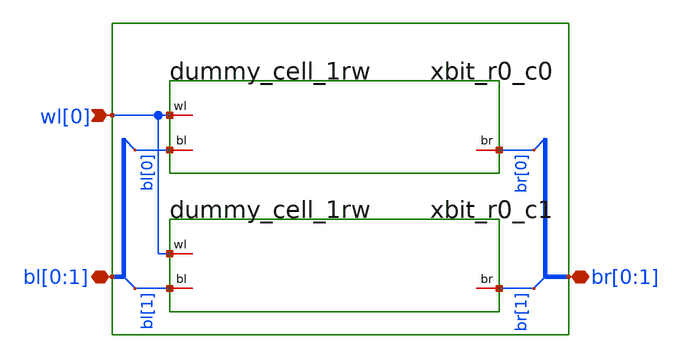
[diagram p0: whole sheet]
** sch_path: sram_2_16_scn4m/dummy_array_1.sch
**.subckt dummy_array_1 bl[0],bl[1] br[0],br[1] wl[0]
*.iopin bl[0],bl[1]
*.iopin br[0],br[1]
*.ipin wl[0]
xbit_r0_c0 bl[0] br[0] wl[0] vdd gnd dummy_cell_1rw
xbit_r0_c1 bl[1] br[1] wl[0] vdd gnd dummy_cell_1rw
**.ends

* expanding   symbol:  dummy_cell_1rw.sym # of pins=3
** sym_path: sram_2_64_scn4m/dummy_cell_1rw.sym
** sch_path: sram_2_64_scn4m/dummy_cell_1rw.sch
.subckt dummy_cell_1rw bl br wl vdd gnd
*.iopin bl
*.iopin br
*.iopin wl
M1004 Q wl bl_noconn gnd n w=0.8u l=0.4u m=1
M1001 Q_bar Q vdd vdd p w=0.6u l=0.8u m=1
M1003 Q_bar Q gnd gnd n w=1.6u l=0.4u m=1
M1002 Q Q_bar gnd gnd n w=1.6u l=0.4u m=1
M1000 Q Q_bar vdd vdd p w=0.6u l=0.8u m=1
M1005 br_noconn wl Q_bar gnd n w=0.8u l=0.4u m=1
* noconn bl_noconn
* noconn br_noconn
* noconn br
* noconn bl
.ends

.end
